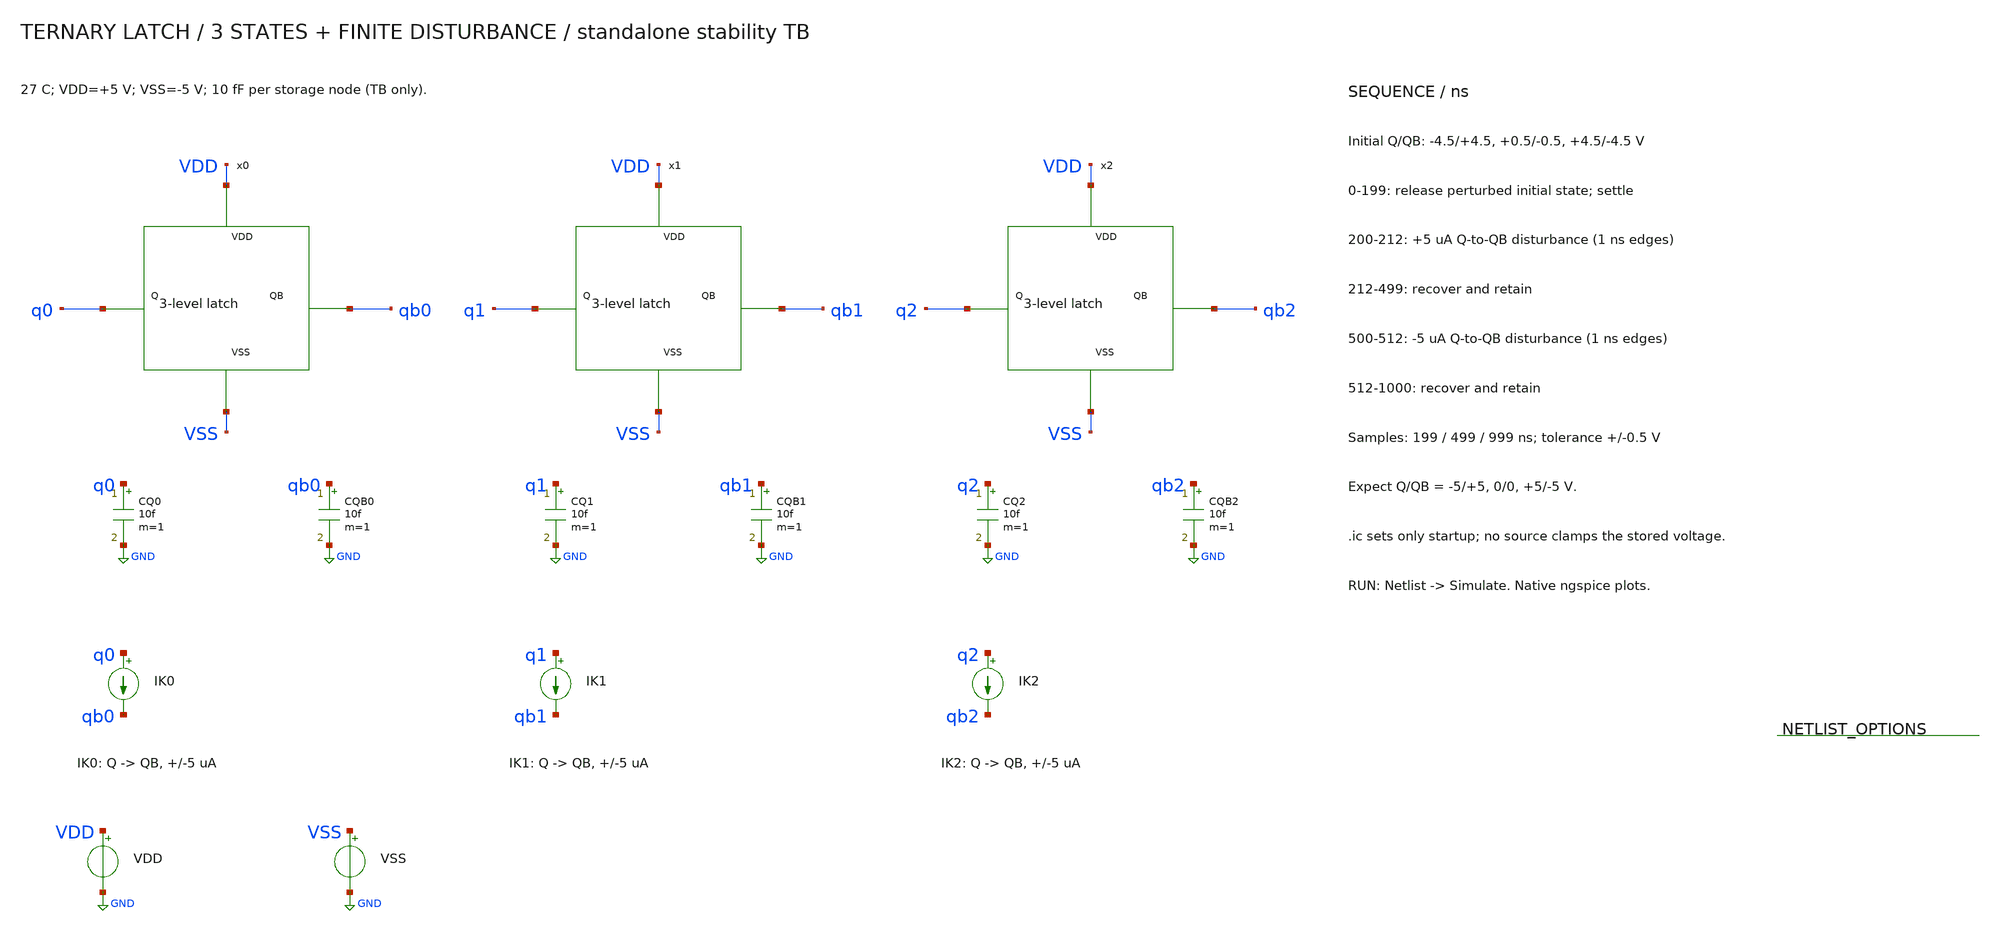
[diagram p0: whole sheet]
** sch_path: member_project/balanced-ternary-logic/PenguinEino/ternary_latch_tb.sch
**.subckt ternary_latch_tb
x0 q0 qb0 VDD VSS ternary_latch
CQ0 q0 GND 10f m=1
CQB0 qb0 GND 10f m=1
IK0 q0 qb0 PWL(0 0 200n 0 201n 5u 211n 5u 212n 0 500n 0 501n -5u 511n -5u 512n 0 1u 0)
x1 q1 qb1 VDD VSS ternary_latch
CQ1 q1 GND 10f m=1
CQB1 qb1 GND 10f m=1
IK1 q1 qb1 PWL(0 0 200n 0 201n 5u 211n 5u 212n 0 500n 0 501n -5u 511n -5u 512n 0 1u 0)
x2 q2 qb2 VDD VSS ternary_latch
CQ2 q2 GND 10f m=1
CQB2 qb2 GND 10f m=1
IK2 q2 qb2 PWL(0 0 200n 0 201n 5u 211n 5u 212n 0 500n 0 501n -5u 511n -5u 512n 0 1u 0)
VDD VDD GND 5
VSS VSS GND -5
**** begin user architecture code
 .include $::LIB/ip62_models

.temp 27
.ic v(q0)=-4.5 v(qb0)=4.5 v(q1)=0.5 v(qb1)=-0.5 v(q2)=4.5 v(qb2)=-4.5
.control
save all
set wr_singlescale
set wr_vecnames
setplot const
let failures=0
tran 0.2n 1000n 0 0.5n
meas tran q0_199 find v(q0) at=199n
if abs(q0_199-(-5)) > 0.5
let const.failures=const.failures+1
echo FAIL: q0_199 expected -5 V
end
meas tran qb0_199 find v(qb0) at=199n
if abs(qb0_199-(5)) > 0.5
let const.failures=const.failures+1
echo FAIL: qb0_199 expected 5 V
end
meas tran q0_499 find v(q0) at=499n
if abs(q0_499-(-5)) > 0.5
let const.failures=const.failures+1
echo FAIL: q0_499 expected -5 V
end
meas tran qb0_499 find v(qb0) at=499n
if abs(qb0_499-(5)) > 0.5
let const.failures=const.failures+1
echo FAIL: qb0_499 expected 5 V
end
meas tran q0_999 find v(q0) at=999n
if abs(q0_999-(-5)) > 0.5
let const.failures=const.failures+1
echo FAIL: q0_999 expected -5 V
end
meas tran qb0_999 find v(qb0) at=999n
if abs(qb0_999-(5)) > 0.5
let const.failures=const.failures+1
echo FAIL: qb0_999 expected 5 V
end
plot v(q0) v(qb0) ylimit -5.5 5.5 title 'Latch: stored Q=-5 V, perturb and recover'
meas tran q1_199 find v(q1) at=199n
if abs(q1_199-(0)) > 0.5
let const.failures=const.failures+1
echo FAIL: q1_199 expected 0 V
end
meas tran qb1_199 find v(qb1) at=199n
if abs(qb1_199-(0)) > 0.5
let const.failures=const.failures+1
echo FAIL: qb1_199 expected 0 V
end
meas tran q1_499 find v(q1) at=499n
if abs(q1_499-(0)) > 0.5
let const.failures=const.failures+1
echo FAIL: q1_499 expected 0 V
end
meas tran qb1_499 find v(qb1) at=499n
if abs(qb1_499-(0)) > 0.5
let const.failures=const.failures+1
echo FAIL: qb1_499 expected 0 V
end
meas tran q1_999 find v(q1) at=999n
if abs(q1_999-(0)) > 0.5
let const.failures=const.failures+1
echo FAIL: q1_999 expected 0 V
end
meas tran qb1_999 find v(qb1) at=999n
if abs(qb1_999-(0)) > 0.5
let const.failures=const.failures+1
echo FAIL: qb1_999 expected 0 V
end
plot v(q1) v(qb1) ylimit -5.5 5.5 title 'Latch: stored Q=0 V, perturb and recover'
meas tran q2_199 find v(q2) at=199n
if abs(q2_199-(5)) > 0.5
let const.failures=const.failures+1
echo FAIL: q2_199 expected 5 V
end
meas tran qb2_199 find v(qb2) at=199n
if abs(qb2_199-(-5)) > 0.5
let const.failures=const.failures+1
echo FAIL: qb2_199 expected -5 V
end
meas tran q2_499 find v(q2) at=499n
if abs(q2_499-(5)) > 0.5
let const.failures=const.failures+1
echo FAIL: q2_499 expected 5 V
end
meas tran qb2_499 find v(qb2) at=499n
if abs(qb2_499-(-5)) > 0.5
let const.failures=const.failures+1
echo FAIL: qb2_499 expected -5 V
end
meas tran q2_999 find v(q2) at=999n
if abs(q2_999-(5)) > 0.5
let const.failures=const.failures+1
echo FAIL: q2_999 expected 5 V
end
meas tran qb2_999 find v(qb2) at=999n
if abs(qb2_999-(-5)) > 0.5
let const.failures=const.failures+1
echo FAIL: qb2_999 expected -5 V
end
plot v(q2) v(qb2) ylimit -5.5 5.5 title 'Latch: stored Q=5 V, perturb and recover'
wrdata ternary_latch_hold.txt v(q0) v(qb0) v(q1) v(qb1) v(q2) v(qb2)
if const.failures = 0
echo PASS: three-state hold and disturbance recovery
else
echo FAIL: three-state hold and disturbance recovery
end
print const.failures
.endc

**** end user architecture code
**.ends

* expanding   symbol:  /home/ishi-kai/balanced-ternary-logic/ternary_latch.sym # of pins=4
** sym_path: member_project/balanced-ternary-logic/PenguinEino/ternary_latch.sym
** sch_path: member_project/balanced-ternary-logic/PenguinEino/ternary_latch.sch
.subckt ternary_latch Q QB VDD VSS
*.opin Q
*.opin QB
*.iopin VDD
*.iopin VSS
x_q QB Q VDD VSS inverter
x_qb Q QB VDD VSS inverter
.ends


* expanding   symbol:  /home/ishi-kai/balanced-ternary-logic/inverter.sym # of pins=4
** sym_path: member_project/balanced-ternary-logic/PenguinEino/inverter.sym
** sch_path: member_project/balanced-ternary-logic/PenguinEino/inverter.sch
.subckt inverter vin vout VDD VSS
*.iopin VDD
*.ipin vin
*.opin vout
*.iopin VSS
XXM1 net1 vin VDD VDD PMOS w=13.5u l=1u nrd=0 nrs=0 m=1
XR1 net1 vout VDD F_RR w=2.8e-06 l=30e-06 R=1 tc1=0 tc2=0 m=1
XR2 vout net2 VDD F_RR w=2.8e-06 l=30e-06 R=1 tc1=0 tc2=0 m=1
XXM2 net2 vin VSS VSS NMOS w=5u l=1u nrd=0 nrs=0 m=1
.ends

.GLOBAL GND
.end
